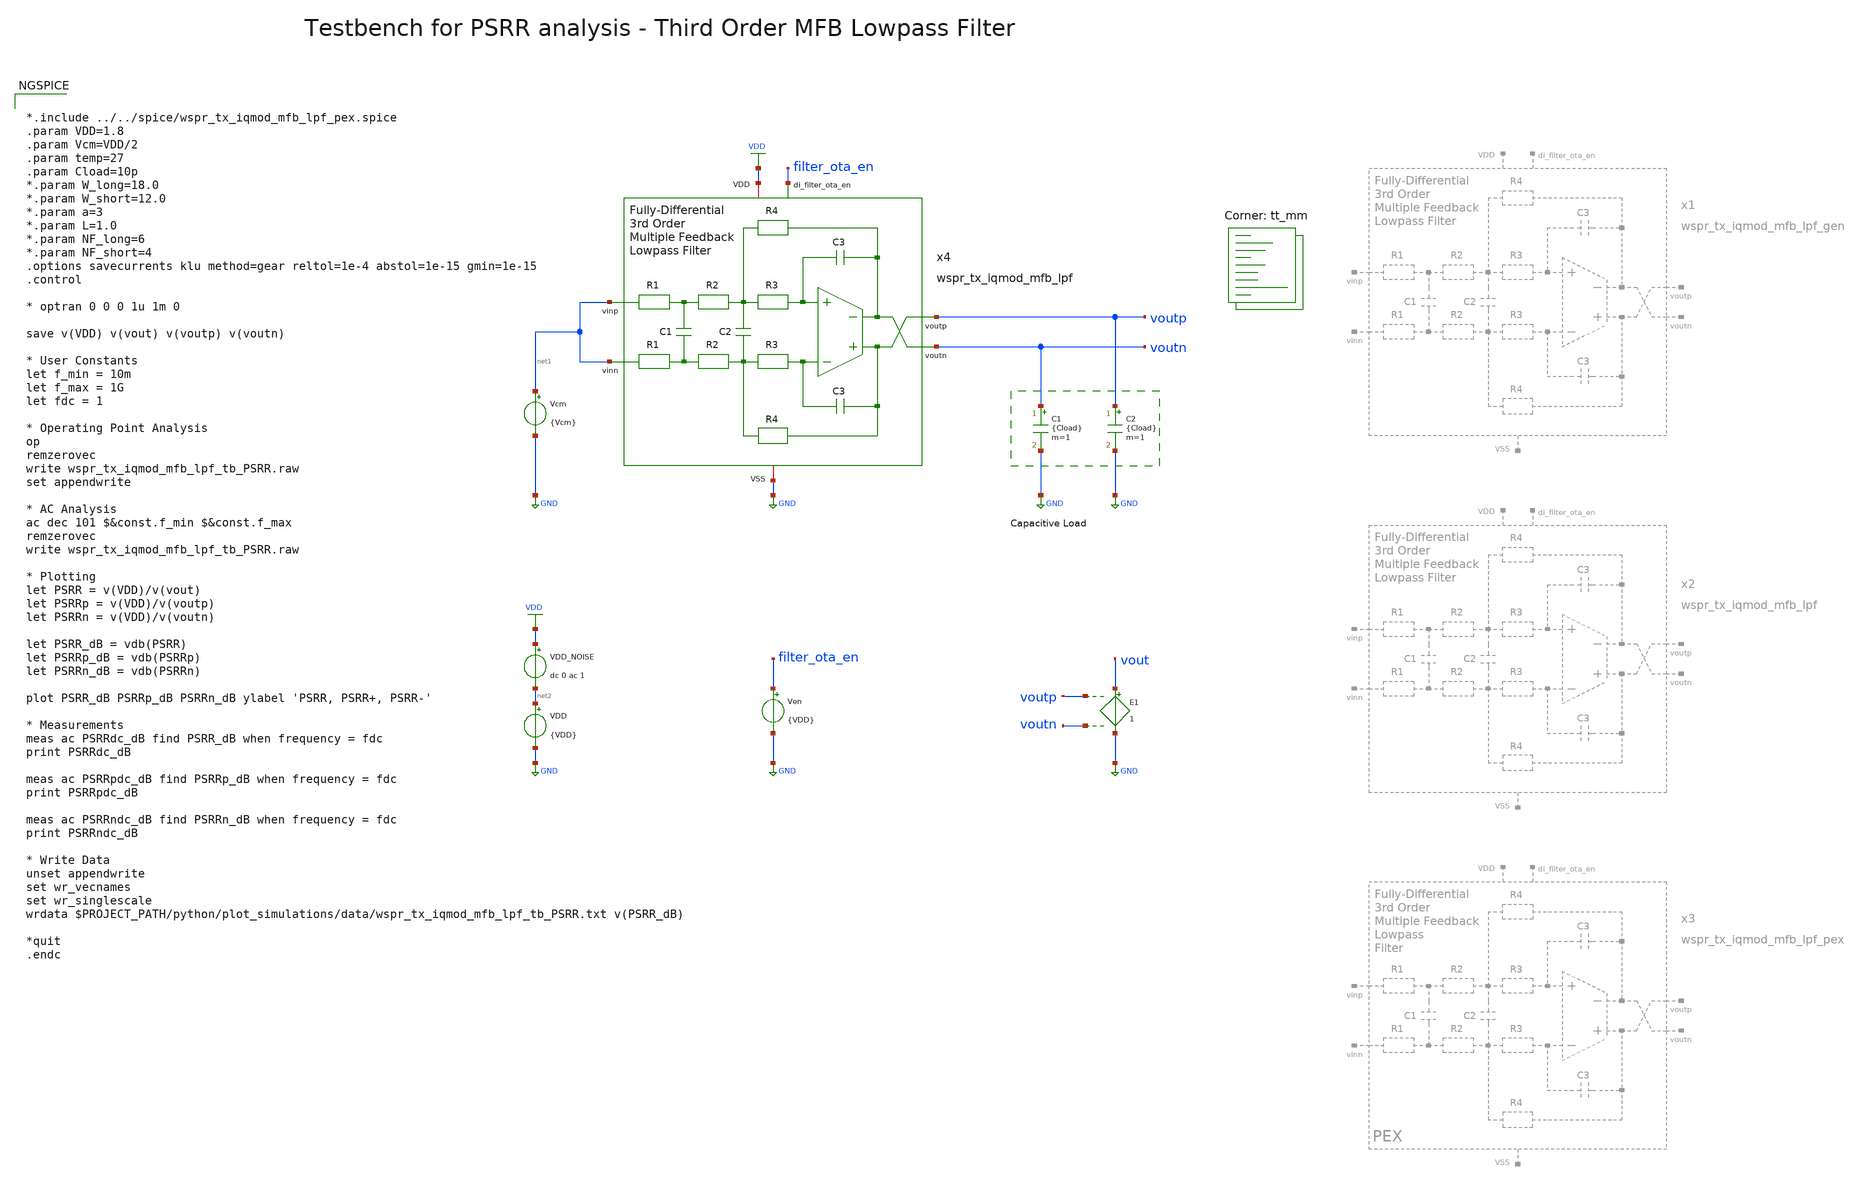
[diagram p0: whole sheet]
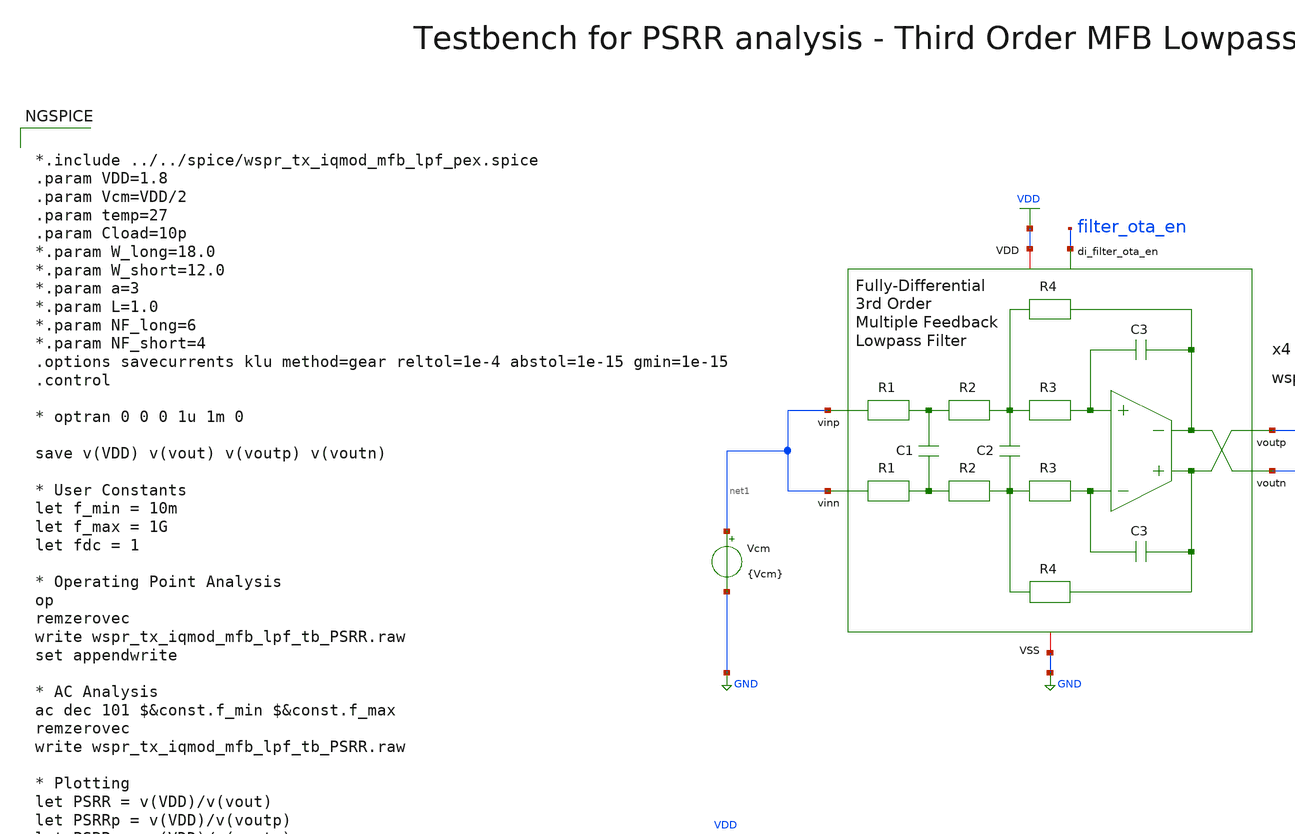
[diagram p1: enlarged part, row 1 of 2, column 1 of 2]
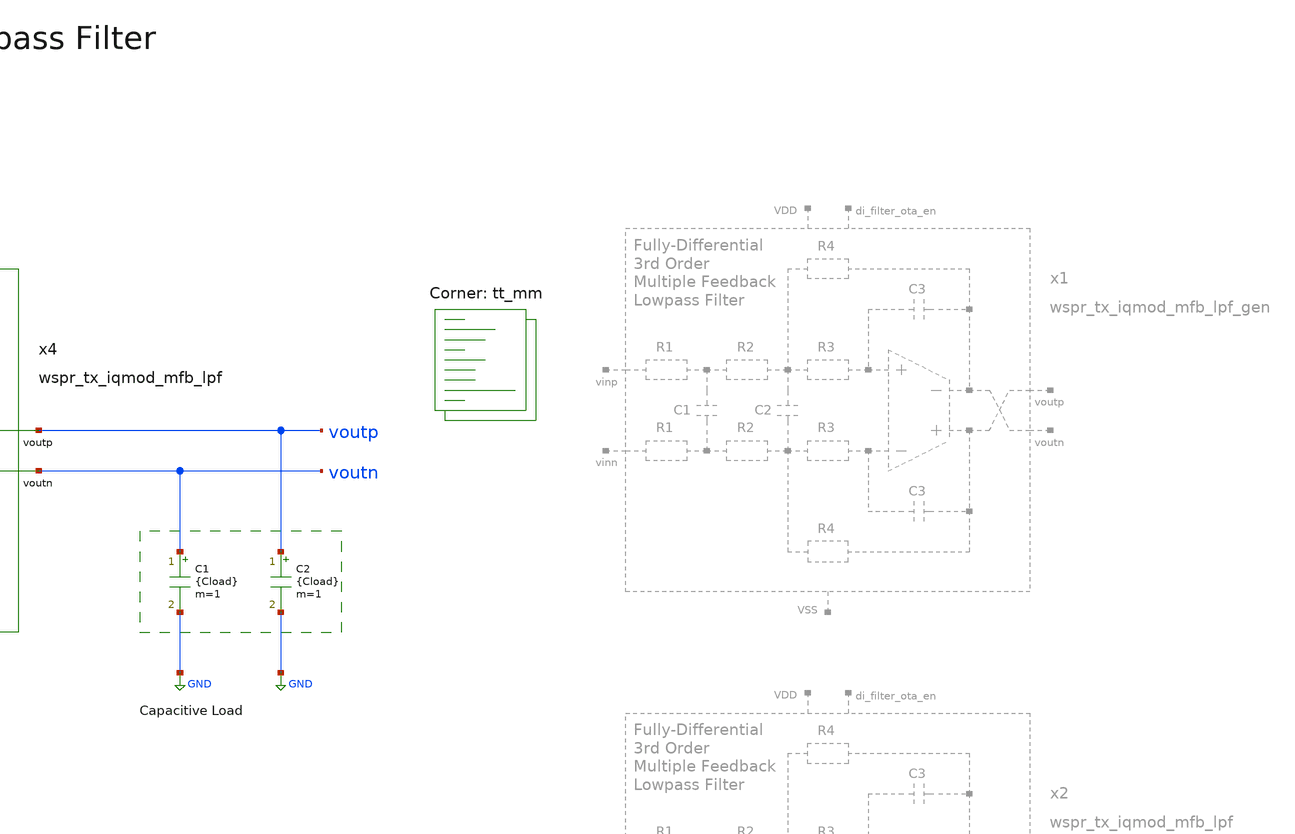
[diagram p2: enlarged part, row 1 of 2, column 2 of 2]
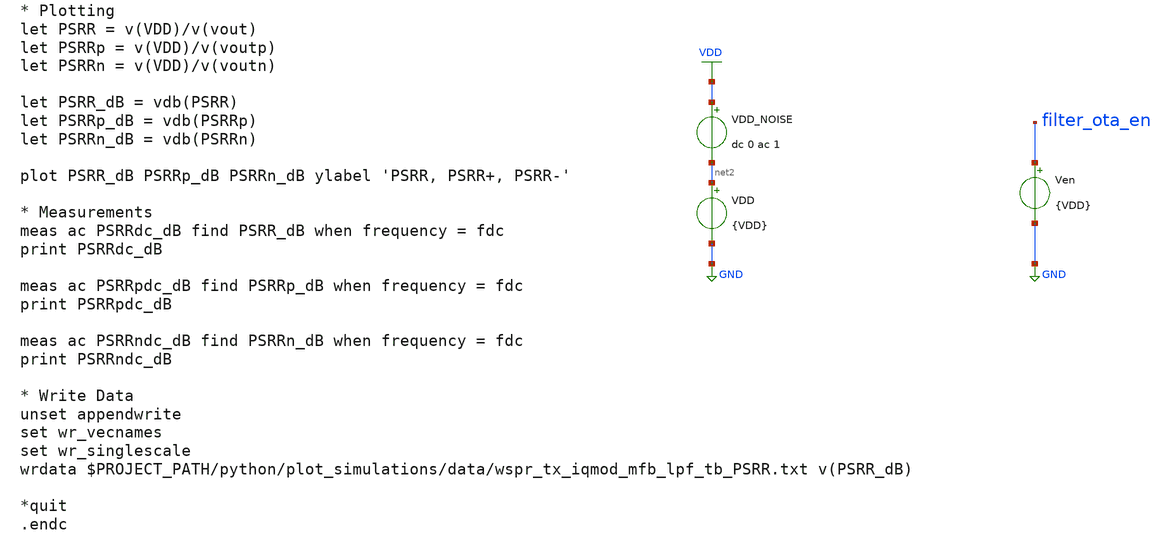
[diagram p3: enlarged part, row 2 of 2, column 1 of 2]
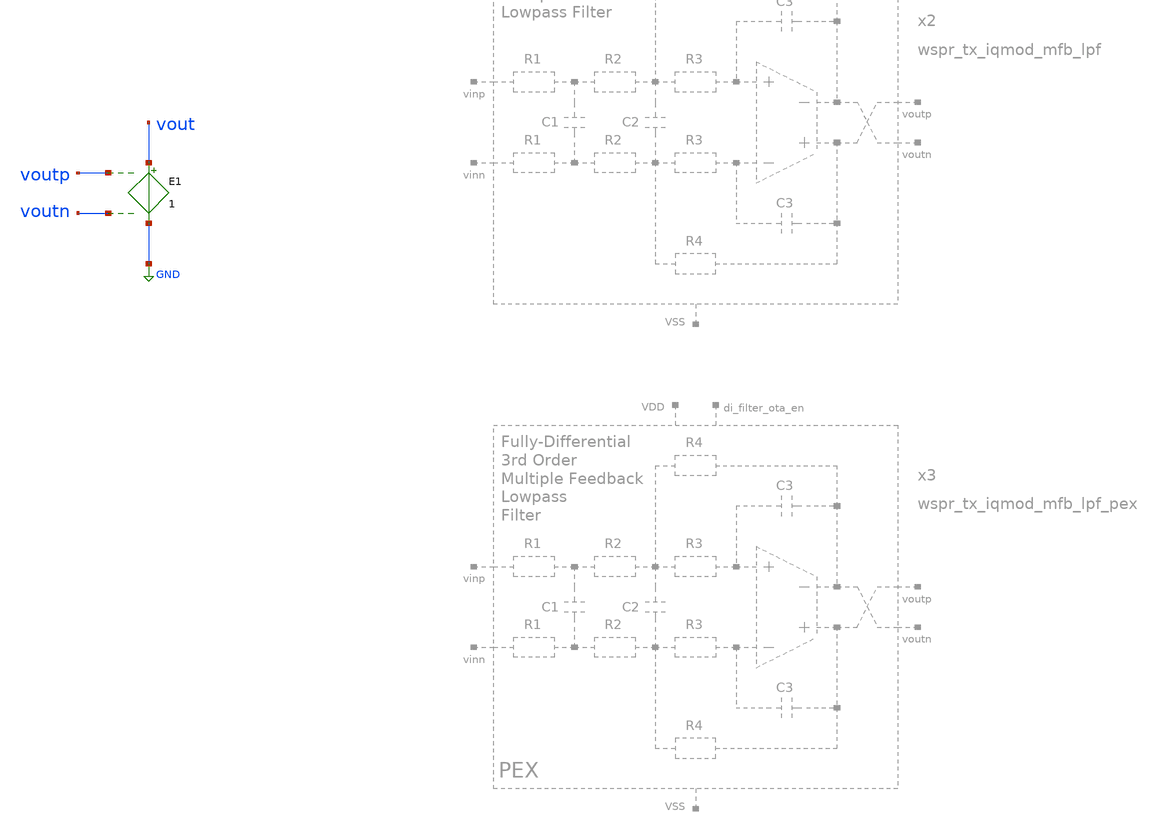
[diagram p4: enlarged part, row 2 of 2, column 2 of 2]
** sch_path: sky130/macros/iqmod/testbenches/wspr_tx_iqmod_mfb_lpf_tb_PSRR.sch
**.subckt wspr_tx_iqmod_mfb_lpf_tb_PSRR
C1 voutn GND {Cload} m=1
C2 voutp GND {Cload} m=1
Vcm net1 GND {Vcm}
E1 vout GND voutp voutn 1
VDD net2 GND {VDD}
VDD_NOISE VDD net2 dc 0 ac 1
Ven filter_ota_en GND {VDD}
x4 filter_ota_en voutp net1 voutn net1 VDD GND wspr_tx_iqmod_mfb_lpf
**** begin user architecture code


*.include ../../spice/wspr_tx_iqmod_mfb_lpf_pex.spice
.param VDD=1.8
.param Vcm=VDD/2
.param temp=27
.param Cload=10p
*.param W_long=18.0
*.param W_short=12.0
*.param a=3
*.param L=1.0
*.param NF_long=6
*.param NF_short=4
.options savecurrents klu method=gear reltol=1e-4 abstol=1e-15 gmin=1e-15
.control

* optran 0 0 0 1u 1m 0

save v(VDD) v(vout) v(voutp) v(voutn)

* User Constants
let f_min = 10m
let f_max = 1G
let fdc = 1

* Operating Point Analysis
op
remzerovec
write wspr_tx_iqmod_mfb_lpf_tb_PSRR.raw
set appendwrite

* AC Analysis
ac dec 101 $&const.f_min $&const.f_max
remzerovec
write wspr_tx_iqmod_mfb_lpf_tb_PSRR.raw

* Plotting
let PSRR = v(VDD)/v(vout)
let PSRRp = v(VDD)/v(voutp)
let PSRRn = v(VDD)/v(voutn)

let PSRR_dB = vdb(PSRR)
let PSRRp_dB = vdb(PSRRp)
let PSRRn_dB = vdb(PSRRn)

plot PSRR_dB PSRRp_dB PSRRn_dB ylabel 'PSRR, PSRR+, PSRR-'

* Measurements
meas ac PSRRdc_dB find PSRR_dB when frequency = fdc
print PSRRdc_dB

meas ac PSRRpdc_dB find PSRRp_dB when frequency = fdc
print PSRRpdc_dB

meas ac PSRRndc_dB find PSRRn_dB when frequency = fdc
print PSRRndc_dB

* Write Data
unset appendwrite
set wr_vecnames
set wr_singlescale
wrdata $PROJECT_PATH/python/plot_simulations/data/wspr_tx_iqmod_mfb_lpf_tb_PSRR.txt v(PSRR_dB)

*quit
.endc


.lib $::SKYWATER_MODELS/sky130.lib.spice tt_mm
**** end user architecture code
**.ends
.GLOBAL GND
.GLOBAL VDD
.end
